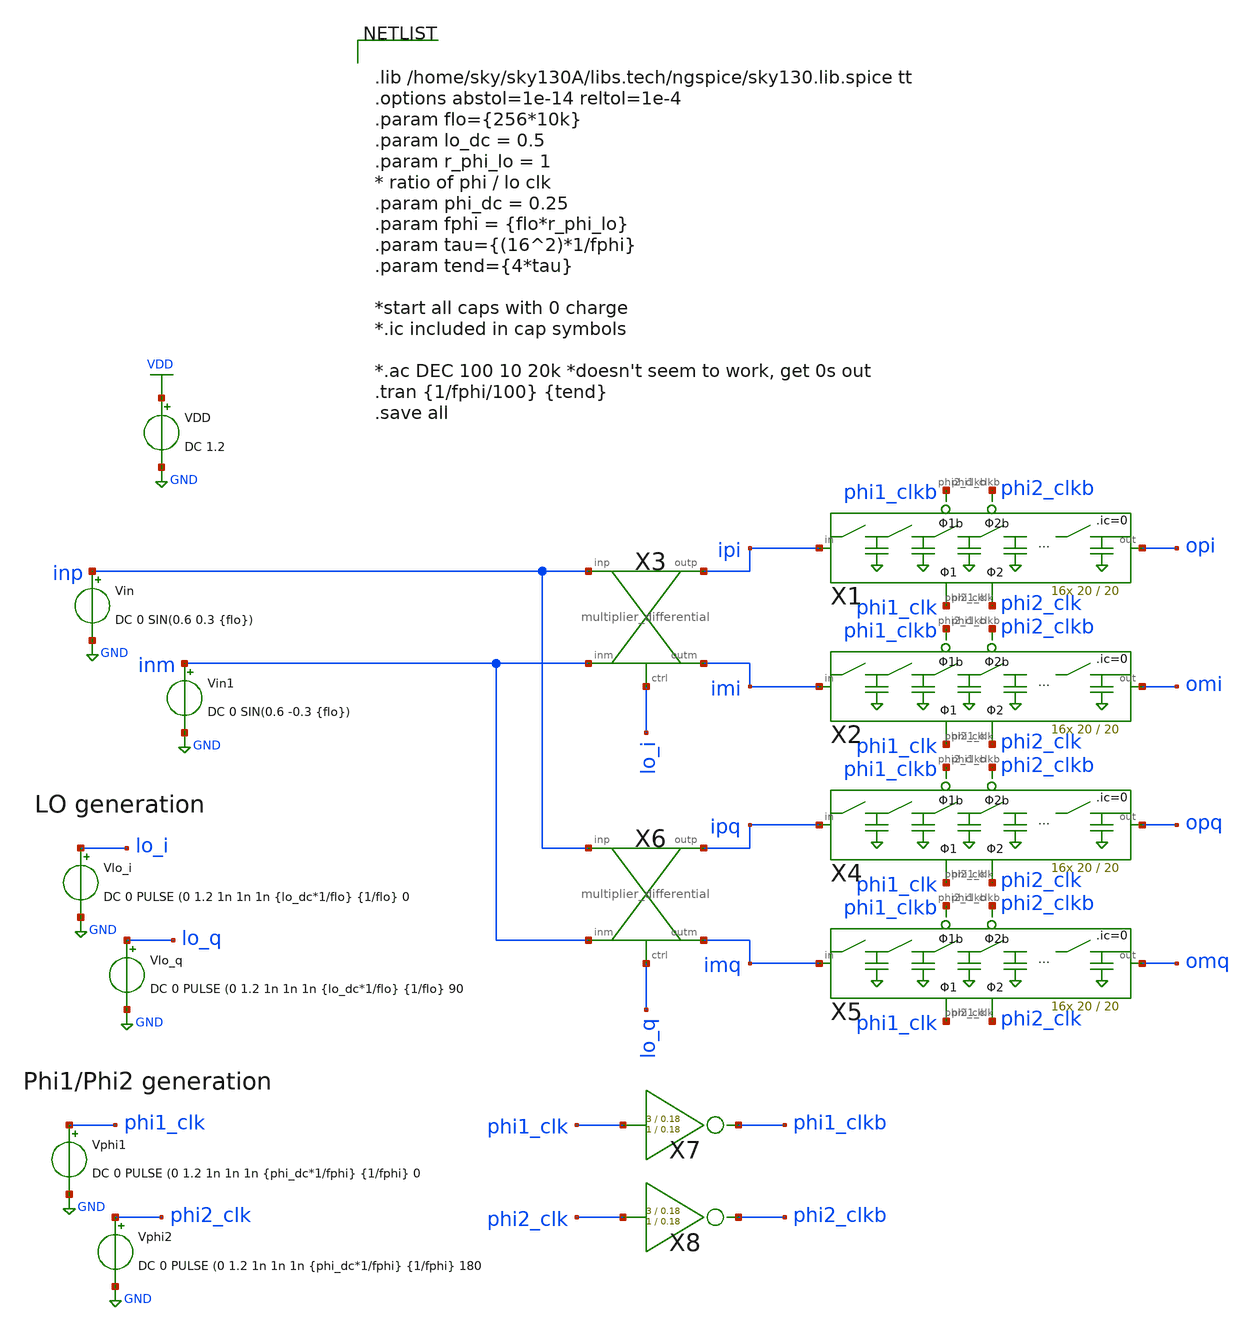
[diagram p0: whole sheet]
** sch_path: xschem/wavelet_channel/wavelet_iq_tb.sch
**.subckt wavelet_iq_tb
Vin inp GND DC 0 SIN(0.6 0.3 {flo})
VDD VDD GND DC 1.2
X8 phi2_clk phi2_clkb inv Wpmos=3 Lpmos=0.18 Wnmos=1 Lnmos=0.18
X3 inp ipi inm lo_i imi multiplier_differential
X6 inp ipq inm lo_q imq multiplier_differential
Vin1 inm GND DC 0 SIN(0.6 -0.3 {flo})
Vlo_i lo_i GND DC 0 PULSE (0 1.2 1n 1n 1n {lo_dc*1/flo} {1/flo} 0
Vlo_q lo_q GND DC 0 PULSE (0 1.2 1n 1n 1n {lo_dc*1/flo} {1/flo} 90
X1 ipi opi phi1_clk phi1_clkb phi2_clk phi2_clkb 16switchcaps_2phi W=20 L=20
X2 imi omi phi1_clk phi1_clkb phi2_clk phi2_clkb 16switchcaps_2phi W=20 L=20
X4 ipq opq phi1_clk phi1_clkb phi2_clk phi2_clkb 16switchcaps_2phi W=20 L=20
X5 imq omq phi1_clk phi1_clkb phi2_clk phi2_clkb 16switchcaps_2phi W=20 L=20
Vphi1 phi1_clk GND DC 0 PULSE (0 1.2 1n 1n 1n {phi_dc*1/fphi} {1/fphi} 0
Vphi2 phi2_clk GND DC 0 PULSE (0 1.2 1n 1n 1n {phi_dc*1/fphi} {1/fphi} 180
X7 phi1_clk phi1_clkb inv Wpmos=3 Lpmos=0.18 Wnmos=1 Lnmos=0.18
**** begin user architecture code


.lib /home/sky/sky130A/libs.tech/ngspice/sky130.lib.spice tt
.options abstol=1e-14 reltol=1e-4
.param flo={256*10k}
.param lo_dc = 0.5
.param r_phi_lo = 1
* ratio of phi / lo clk
.param phi_dc = 0.25
.param fphi = {flo*r_phi_lo}
.param tau={(16^2)*1/fphi}
.param tend={4*tau}

*start all caps with 0 charge
*.ic included in cap symbols

*.ac DEC 100 10 20k *doesn't seem to work, get 0s out
.tran {1/fphi/100} {tend}
.save all


**** end user architecture code
**.ends
.GLOBAL GND
.GLOBAL VDD
.end
